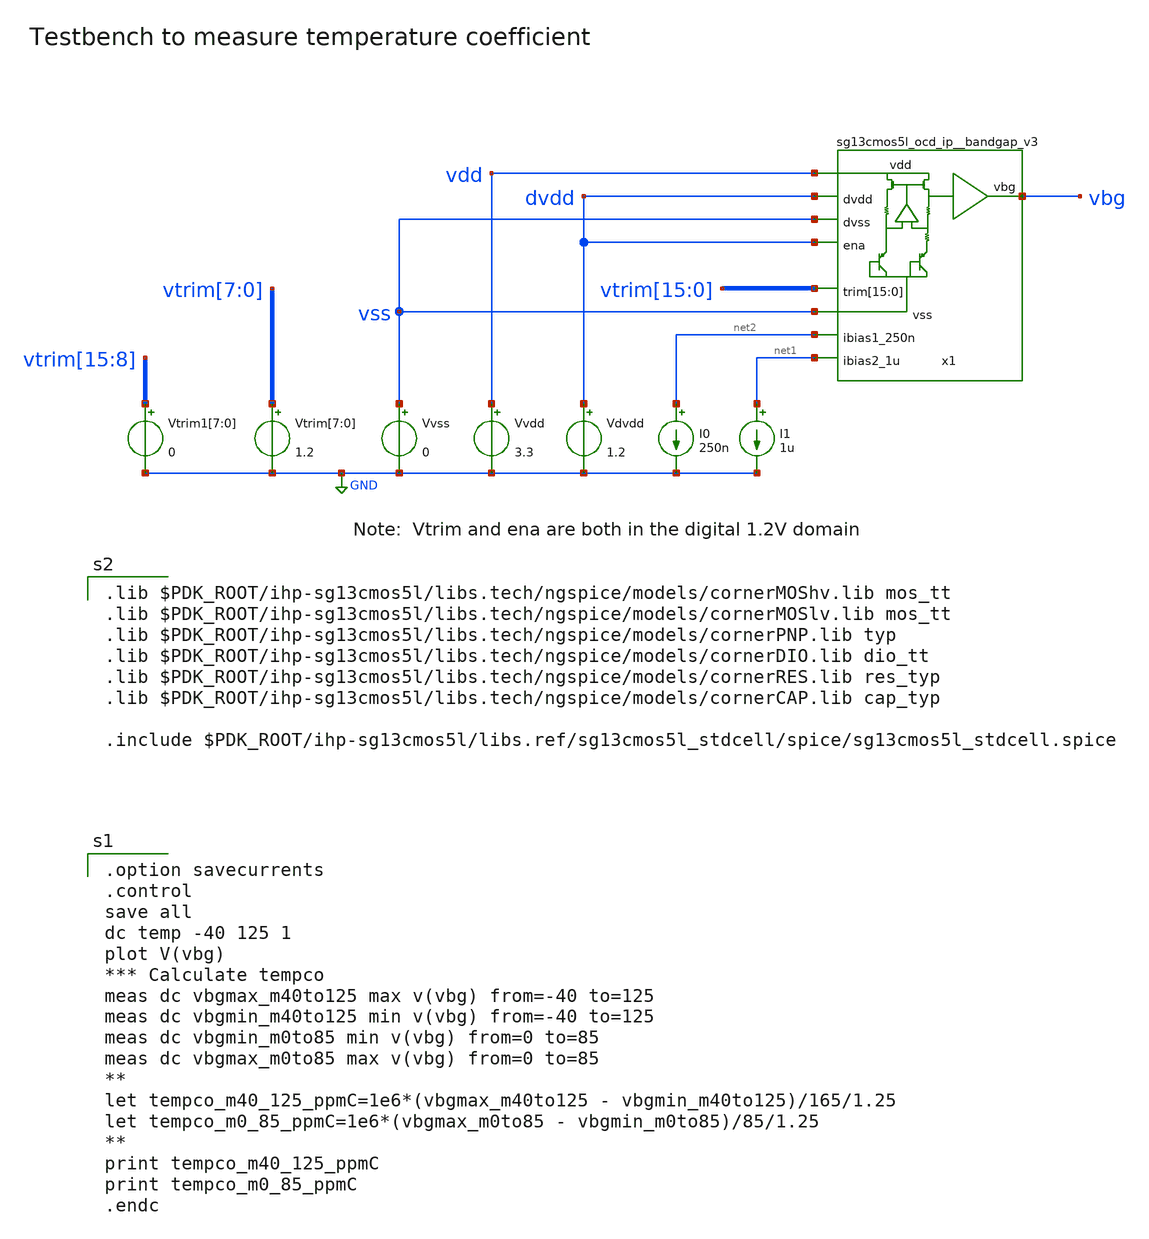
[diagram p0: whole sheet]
** sch_path: xschem/bandgap_tc_tb.sch
**.subckt bandgap_tc_tb
Vvss vss GND 0
Vtrim[7] vtrim[7] GND 1.2
Vtrim[6] vtrim[6] GND 1.2
Vtrim[5] vtrim[5] GND 1.2
Vtrim[4] vtrim[4] GND 1.2
Vtrim[3] vtrim[3] GND 1.2
Vtrim[2] vtrim[2] GND 1.2
Vtrim[1] vtrim[1] GND 1.2
Vtrim[0] vtrim[0] GND 1.2
Vvdd vdd GND 3.3
I0 net2 GND 250n
Vdvdd dvdd GND 1.2
I1 net1 GND 1u
Vtrim1[7] vtrim[15] GND 0
Vtrim1[6] vtrim[14] GND 0
Vtrim1[5] vtrim[13] GND 0
Vtrim1[4] vtrim[12] GND 0
Vtrim1[3] vtrim[11] GND 0
Vtrim1[2] vtrim[10] GND 0
Vtrim1[1] vtrim[9] GND 0
Vtrim1[0] vtrim[8] GND 0
x1 vdd vbg vss net2 vtrim[15] vtrim[14] vtrim[13] vtrim[12] vtrim[11] vtrim[10] vtrim[9] vtrim[8]
+ vtrim[7] vtrim[6] vtrim[5] vtrim[4] vtrim[3] vtrim[2] vtrim[1] vtrim[0] vss dvdd dvdd net1
+ sg13cmos5l_ocd_ip__bandgap_v3
**** begin user architecture code

.option savecurrents
.control
save all
dc temp -40 125 1
plot V(vbg)
*** Calculate tempco
meas dc vbgmax_m40to125 max v(vbg) from=-40 to=125
meas dc vbgmin_m40to125 min v(vbg) from=-40 to=125
meas dc vbgmin_m0to85 min v(vbg) from=0 to=85
meas dc vbgmax_m0to85 max v(vbg) from=0 to=85
**
let tempco_m40_125_ppmC=1e6*(vbgmax_m40to125 - vbgmin_m40to125)/165/1.25
let tempco_m0_85_ppmC=1e6*(vbgmax_m0to85 - vbgmin_m0to85)/85/1.25
**
print tempco_m40_125_ppmC
print tempco_m0_85_ppmC
.endc


.lib $PDK_ROOT/ihp-sg13cmos5l/libs.tech/ngspice/models/cornerMOShv.lib mos_tt
.lib $PDK_ROOT/ihp-sg13cmos5l/libs.tech/ngspice/models/cornerMOSlv.lib mos_tt
.lib $PDK_ROOT/ihp-sg13cmos5l/libs.tech/ngspice/models/cornerPNP.lib typ
.lib $PDK_ROOT/ihp-sg13cmos5l/libs.tech/ngspice/models/cornerDIO.lib dio_tt
.lib $PDK_ROOT/ihp-sg13cmos5l/libs.tech/ngspice/models/cornerRES.lib res_typ
.lib $PDK_ROOT/ihp-sg13cmos5l/libs.tech/ngspice/models/cornerCAP.lib cap_typ

.include $PDK_ROOT/ihp-sg13cmos5l/libs.ref/sg13cmos5l_stdcell/spice/sg13cmos5l_stdcell.spice


**** end user architecture code
**.ends
.GLOBAL GND
.end
